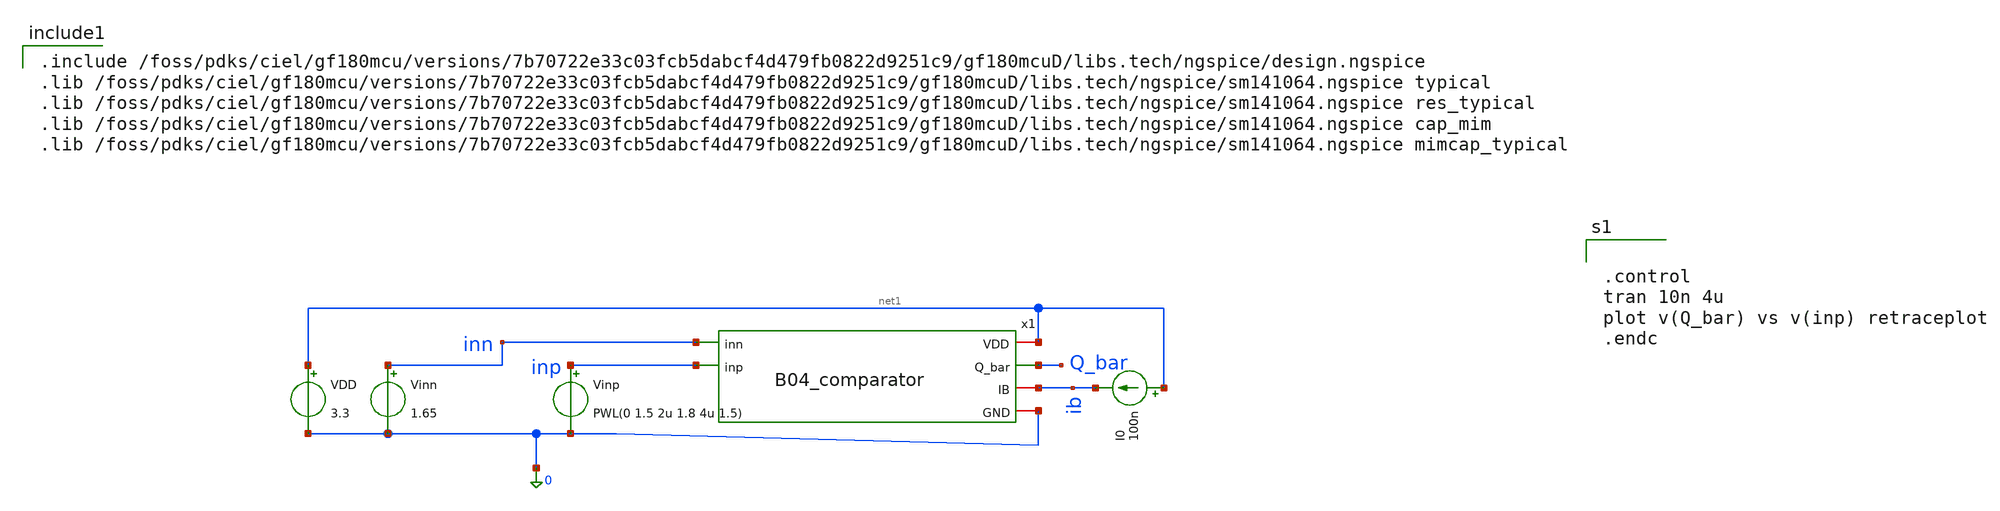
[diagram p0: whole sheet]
** sch_path: analog/B04_tb_comparator.sch
**.subckt B04_tb_comparator
Vinn inn 0 1.65
VDD net1 0 3.3
Vinp inp 0 PWL(0 1.5 2u 1.8 4u 1.5)
I0 net1 ib 100n
x1 net1 Q_bar inn inp ib 0 B04_comparator
**** begin user architecture code

.include /foss/pdks/ciel/gf180mcu/versions/7b70722e33c03fcb5dabcf4d479fb0822d9251c9/gf180mcuD/libs.tech/ngspice/design.ngspice
.lib /foss/pdks/ciel/gf180mcu/versions/7b70722e33c03fcb5dabcf4d479fb0822d9251c9/gf180mcuD/libs.tech/ngspice/sm141064.ngspice typical
.lib /foss/pdks/ciel/gf180mcu/versions/7b70722e33c03fcb5dabcf4d479fb0822d9251c9/gf180mcuD/libs.tech/ngspice/sm141064.ngspice res_typical
.lib /foss/pdks/ciel/gf180mcu/versions/7b70722e33c03fcb5dabcf4d479fb0822d9251c9/gf180mcuD/libs.tech/ngspice/sm141064.ngspice cap_mim
.lib /foss/pdks/ciel/gf180mcu/versions/7b70722e33c03fcb5dabcf4d479fb0822d9251c9/gf180mcuD/libs.tech/ngspice/sm141064.ngspice mimcap_typical



.control
tran 10n 4u
plot v(Q_bar) vs v(inp) retraceplot
.endc


**** end user architecture code
**.ends

* expanding   symbol:
*+  AURA-Event-Driven-Mixed-Signal-ASIC-for-Acoustic-Pattern-Detection/analog/B04_comparator.sym # of pins=6
** sym_path: analog/B04_comparator.sym
** sch_path: analog/B04_comparator.sch
.subckt B04_comparator VDD Q_bar inn inp IB GND
*.iopin VDD
*.iopin GND
*.ipin INN
*.ipin INP
*.iopin IB
*.opin Q_BAR
XM1 net2 IB GND GND nfet_03v3 L=0.56u W=1u nf=1 ad='int((nf+1)/2) * W/nf * 0.18u' as='int((nf+2)/2) * W/nf * 0.18u'
+ pd='2*int((nf+1)/2) * (W/nf + 0.18u)' ps='2*int((nf+2)/2) * (W/nf + 0.18u)' nrd='0.18u / W' nrs='0.18u / W'
+ sa=0 sb=0 sd=0 m=1
XM2 IB IB GND GND nfet_03v3 L=0.56u W=1u nf=1 ad='int((nf+1)/2) * W/nf * 0.18u' as='int((nf+2)/2) * W/nf * 0.18u'
+ pd='2*int((nf+1)/2) * (W/nf + 0.18u)' ps='2*int((nf+2)/2) * (W/nf + 0.18u)' nrd='0.18u / W' nrs='0.18u / W'
+ sa=0 sb=0 sd=0 m=1
XM3 net1 net1 GND GND nfet_03v3 L=0.56u W=1u nf=1 ad='int((nf+1)/2) * W/nf * 0.18u' as='int((nf+2)/2) * W/nf * 0.18u'
+ pd='2*int((nf+1)/2) * (W/nf + 0.18u)' ps='2*int((nf+2)/2) * (W/nf + 0.18u)' nrd='0.18u / W' nrs='0.18u / W'
+ sa=0 sb=0 sd=0 m=1
XMqqq net3 INN net2 GND nfet_03v3 L=0.28u W=2u nf=1 ad='int((nf+1)/2) * W/nf * 0.18u' as='int((nf+2)/2) * W/nf * 0.18u'
+ pd='2*int((nf+1)/2) * (W/nf + 0.18u)' ps='2*int((nf+2)/2) * (W/nf + 0.18u)' nrd='0.18u / W' nrs='0.18u / W'
+ sa=0 sb=0 sd=0 m=1
XMqqq1 net4 INP net2 GND nfet_03v3 L=0.28u W=2u nf=1 ad='int((nf+1)/2) * W/nf * 0.18u' as='int((nf+2)/2) * W/nf * 0.18u'
+ pd='2*int((nf+1)/2) * (W/nf + 0.18u)' ps='2*int((nf+2)/2) * (W/nf + 0.18u)' nrd='0.18u / W' nrs='0.18u / W'
+ sa=0 sb=0 sd=0 m=1
XM6 Q_BAR net1 GND GND nfet_03v3 L=0.56u W=1u nf=1 ad='int((nf+1)/2) * W/nf * 0.18u' as='int((nf+2)/2) * W/nf * 0.18u'
+ pd='2*int((nf+1)/2) * (W/nf + 0.18u)' ps='2*int((nf+2)/2) * (W/nf + 0.18u)' nrd='0.18u / W' nrs='0.18u / W'
+ sa=0 sb=0 sd=0 m=1
XMq0 net3 net3 VDD VDD pfet_03v3 L=0.28u W=1.5u nf=1 ad='int((nf+1)/2) * W/nf * 0.18u' as='int((nf+2)/2) * W/nf * 0.18u'
+ pd='2*int((nf+1)/2) * (W/nf + 0.18u)' ps='2*int((nf+2)/2) * (W/nf + 0.18u)' nrd='0.18u / W' nrs='0.18u / W'
+ sa=0 sb=0 sd=0 m=1
XMq1 net1 net3 VDD VDD pfet_03v3 L=0.28u W=1.5u nf=1 ad='int((nf+1)/2) * W/nf * 0.18u' as='int((nf+2)/2) * W/nf * 0.18u'
+ pd='2*int((nf+1)/2) * (W/nf + 0.18u)' ps='2*int((nf+2)/2) * (W/nf + 0.18u)' nrd='0.18u / W' nrs='0.18u / W'
+ sa=0 sb=0 sd=0 m=1
XMq4 net3 net4 VDD VDD pfet_03v3 L=0.28u W=3.5u nf=1 ad='int((nf+1)/2) * W/nf * 0.18u' as='int((nf+2)/2) * W/nf * 0.18u'
+ pd='2*int((nf+1)/2) * (W/nf + 0.18u)' ps='2*int((nf+2)/2) * (W/nf + 0.18u)' nrd='0.18u / W' nrs='0.18u / W'
+ sa=0 sb=0 sd=0 m=1
XMq5 net4 net3 VDD VDD pfet_03v3 L=0.28u W=3.5u nf=1 ad='int((nf+1)/2) * W/nf * 0.18u' as='int((nf+2)/2) * W/nf * 0.18u'
+ pd='2*int((nf+1)/2) * (W/nf + 0.18u)' ps='2*int((nf+2)/2) * (W/nf + 0.18u)' nrd='0.18u / W' nrs='0.18u / W'
+ sa=0 sb=0 sd=0 m=1
XMq2 net4 net4 VDD VDD pfet_03v3 L=0.28u W=1.5u nf=1 ad='int((nf+1)/2) * W/nf * 0.18u' as='int((nf+2)/2) * W/nf * 0.18u'
+ pd='2*int((nf+1)/2) * (W/nf + 0.18u)' ps='2*int((nf+2)/2) * (W/nf + 0.18u)' nrd='0.18u / W' nrs='0.18u / W'
+ sa=0 sb=0 sd=0 m=1
XMq3 Q_BAR net4 VDD VDD pfet_03v3 L=0.28u W=1.5u nf=1 ad='int((nf+1)/2) * W/nf * 0.18u' as='int((nf+2)/2) * W/nf * 0.18u'
+ pd='2*int((nf+1)/2) * (W/nf + 0.18u)' ps='2*int((nf+2)/2) * (W/nf + 0.18u)' nrd='0.18u / W' nrs='0.18u / W'
+ sa=0 sb=0 sd=0 m=1
.ends

.end
